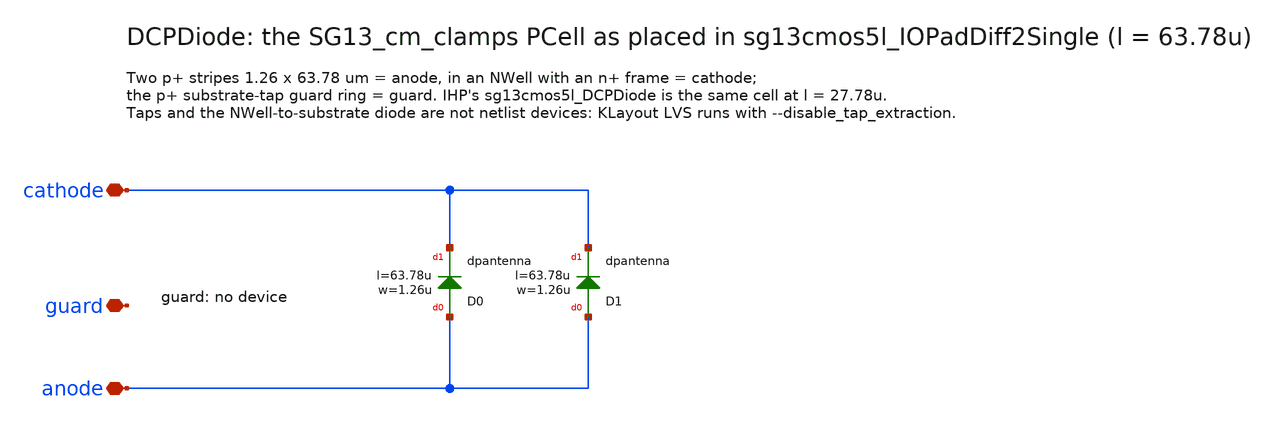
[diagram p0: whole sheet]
** sch_path: macros/IOPad/schematic/xschem/DCPDiode.sch
**.subckt DCPDiode anode cathode guard
*.iopin anode
*.iopin cathode
*.iopin guard
XD0 anode cathode dpantenna l=63.78u w=1.26u
XD1 anode cathode dpantenna l=63.78u w=1.26u
**.ends
.end
